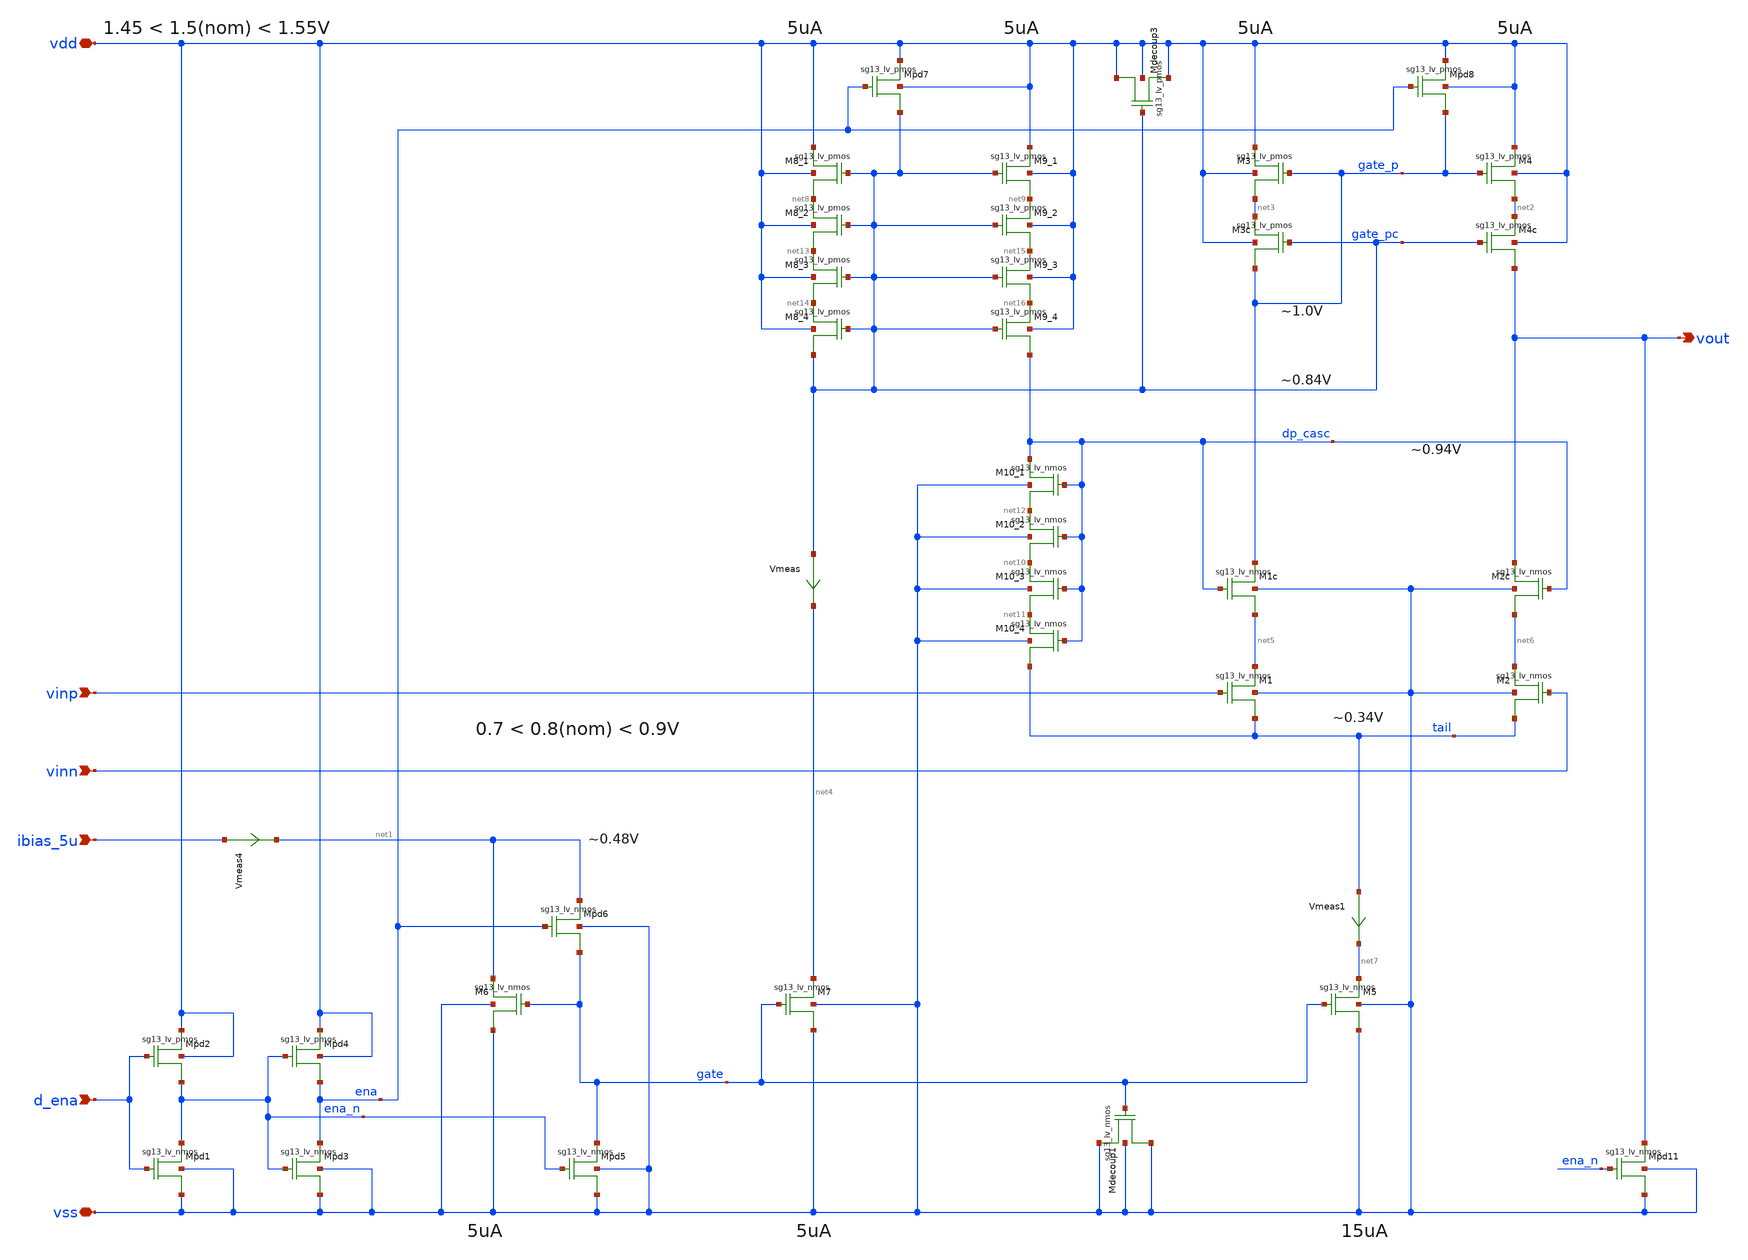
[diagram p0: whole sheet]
** sch_path: xschem/ota-improved.sch
* (c) 2024-2025 Harald Pretl, Apache-2.0 license
**.subckt ota-improved ibias_5u vdd vss vinp vinn vout d_ena
*.ipin ibias_5u
*.iopin vdd
*.iopin vss
*.ipin vinp
*.ipin vinn
*.opin vout
*.ipin d_ena
XM5 net7 gate vss vss sg13_lv_nmos w=6u l=5u ng=3 m=1
XM4 vdd gate_p net2 vdd sg13_lv_pmos w=3u l=0.5u ng=1 m=1
XM1 net5 vinp tail vss sg13_lv_nmos w=1u l=0.5u ng=1 m=1
XM2 net6 vinn tail vss sg13_lv_nmos w=1u l=0.5u ng=1 m=1
XM3 vdd gate_p net3 vdd sg13_lv_pmos w=3u l=0.5u ng=1 m=1
XM6 net1 gate vss vss sg13_lv_nmos w=2u l=5u ng=1 m=1
XMpd5 gate ena_n vss vss sg13_lv_nmos w=1u l=0.13u ng=1 m=1
XMpd3 ena ena_n vss vss sg13_lv_nmos w=1u l=0.13u ng=1 m=1
XMpd4 vdd ena_n ena vdd sg13_lv_pmos w=1u l=0.13u ng=1 m=1
XMpd6 net1 ena gate vss sg13_lv_nmos w=1u l=0.13u ng=1 m=1
XM2c vout dp_casc net6 vss sg13_lv_nmos w=1u l=0.5u ng=1 m=1
XM1c gate_p dp_casc net5 vss sg13_lv_nmos w=1u l=0.5u ng=1 m=1
XM4c net2 gate_pc vout vdd sg13_lv_pmos w=3u l=0.5u ng=1 m=1
XM3c net3 gate_pc gate_p vdd sg13_lv_pmos w=3u l=0.5u ng=1 m=1
XM7 net4 gate vss vss sg13_lv_nmos w=2u l=5u ng=1 m=1
XMpd8 vdd ena gate_p vdd sg13_lv_pmos w=1u l=0.13u ng=1 m=1
XM8_1 vdd gate_pc net8 vdd sg13_lv_pmos w=3u l=0.5u ng=1 m=1
XM9_1 vdd gate_pc net9 vdd sg13_lv_pmos w=3u l=0.5u ng=1 m=1
XMpd7 vdd ena gate_pc vdd sg13_lv_pmos w=1u l=0.13u ng=1 m=1
XM10_3 net10 dp_casc net11 vss sg13_lv_nmos w=1u l=0.5u ng=1 m=1
Vmeas gate_pc net4 0
.save i(vmeas)
Vmeas1 tail net7 0
.save i(vmeas1)
XMpd1 ena_n d_ena vss vss sg13_lv_nmos w=1u l=0.13u ng=1 m=1
XMpd2 vdd d_ena ena_n vdd sg13_lv_pmos w=1u l=0.13u ng=1 m=1
Vmeas4 ibias_5u net1 0
.save i(vmeas4)
XMpd11 vout ena_n vss vss sg13_lv_nmos w=0.5u l=0.13u ng=1 m=1
XM10_4 net11 dp_casc tail vss sg13_lv_nmos w=1u l=0.5u ng=1 m=1
XMdecoup1 vss gate vss vss sg13_lv_nmos w=8u l=1u ng=4 m=1
XMdecoup3 vdd gate_pc vdd vdd sg13_lv_pmos w=12u l=0.5u ng=4 m=1
XM10_2 net12 dp_casc net10 vss sg13_lv_nmos w=1u l=0.5u ng=1 m=1
XM10_1 dp_casc dp_casc net12 vss sg13_lv_nmos w=1u l=0.5u ng=1 m=1
XM8_2 net8 gate_pc net13 vdd sg13_lv_pmos w=3u l=0.5u ng=1 m=1
XM8_3 net13 gate_pc net14 vdd sg13_lv_pmos w=3u l=0.5u ng=1 m=1
XM9_2 net9 gate_pc net15 vdd sg13_lv_pmos w=3u l=0.5u ng=1 m=1
XM9_3 net15 gate_pc net16 vdd sg13_lv_pmos w=3u l=0.5u ng=1 m=1
XM8_4 net14 gate_pc gate_pc vdd sg13_lv_pmos w=3u l=0.5u ng=1 m=1
XM9_4 net16 gate_pc dp_casc vdd sg13_lv_pmos w=3u l=0.5u ng=1 m=1
**.ends
.end
